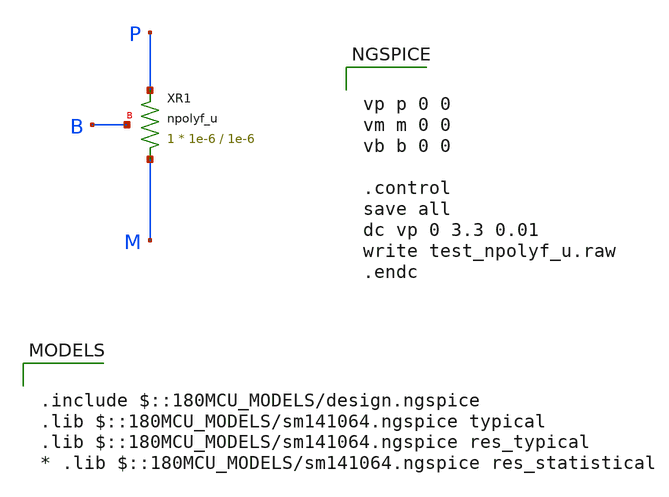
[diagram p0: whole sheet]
** sch_path: gf180mcuD/xschem_libs/gf180mcu_tests/test_npolyf_u/schematic/test_npolyf_u.sch
* Copyright 2022 GlobalFoundries PDK Authors
* Licensed under the Apache License, Version 2.0 (the "License");
* you may not use this file except in compliance with the License.
* You may obtain a copy of the License at
* https://www.apache.org/licenses/LICENSE-2.0
* Unless required by applicable law or agreed to in writing, software
* distributed under the License is distributed on an "AS IS" BASIS,
* WITHOUT WARRANTIES OR CONDITIONS OF ANY KIND, either express or implied.
* See the License for the specific language governing permissions and
* limitations under the License.
**.subckt test_npolyf_u
XR1 M P B npolyf_u r_width=1e-6 r_length=1e-6 m=1
**** begin user architecture code

.include $::180MCU_MODELS/design.ngspice
.lib $::180MCU_MODELS/sm141064.ngspice typical
.lib $::180MCU_MODELS/sm141064.ngspice res_typical
* .lib $::180MCU_MODELS/sm141064.ngspice res_statistical



vp p 0 0
vm m 0 0
vb b 0 0

.control
save all
dc vp 0 3.3 0.01
write test_npolyf_u.raw
.endc


**** end user architecture code
**.ends
.end
